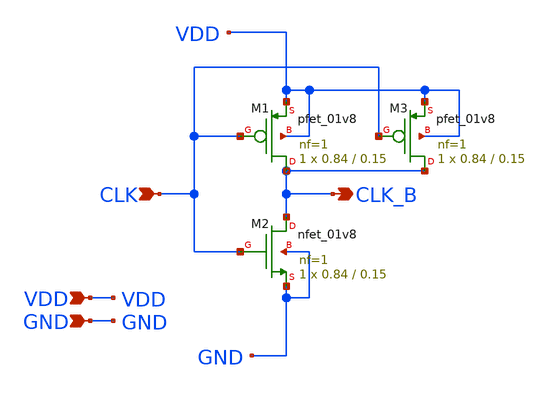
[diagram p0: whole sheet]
** sch_path: xschem/inv_n84_p168.sch
**.subckt inv_n84_p168 CLK_B CLK VDD GND
*.opin CLK_B
*.ipin CLK
*.ipin VDD
*.ipin GND
XM1 CLK_B CLK VDD VDD sky130_fd_pr__pfet_01v8 L=0.15 W=0.84 nf=1 ad='int((nf+1)/2) * W/nf * 0.29' as='int((nf+2)/2) * W/nf * 0.29'
+ pd='2*int((nf+1)/2) * (W/nf + 0.29)' ps='2*int((nf+2)/2) * (W/nf + 0.29)' nrd='0.29 / W' nrs='0.29 / W'
+ sa=0 sb=0 sd=0 mult=1 m=1
XM2 CLK_B CLK GND GND sky130_fd_pr__nfet_01v8 L=0.15 W=0.84 nf=1 ad='int((nf+1)/2) * W/nf * 0.29' as='int((nf+2)/2) * W/nf * 0.29'
+ pd='2*int((nf+1)/2) * (W/nf + 0.29)' ps='2*int((nf+2)/2) * (W/nf + 0.29)' nrd='0.29 / W' nrs='0.29 / W'
+ sa=0 sb=0 sd=0 mult=1 m=1
XM3 CLK_B CLK VDD VDD sky130_fd_pr__pfet_01v8 L=0.15 W=0.84 nf=1 ad='int((nf+1)/2) * W/nf * 0.29' as='int((nf+2)/2) * W/nf * 0.29'
+ pd='2*int((nf+1)/2) * (W/nf + 0.29)' ps='2*int((nf+2)/2) * (W/nf + 0.29)' nrd='0.29 / W' nrs='0.29 / W'
+ sa=0 sb=0 sd=0 mult=1 m=1
**.ends
.end
